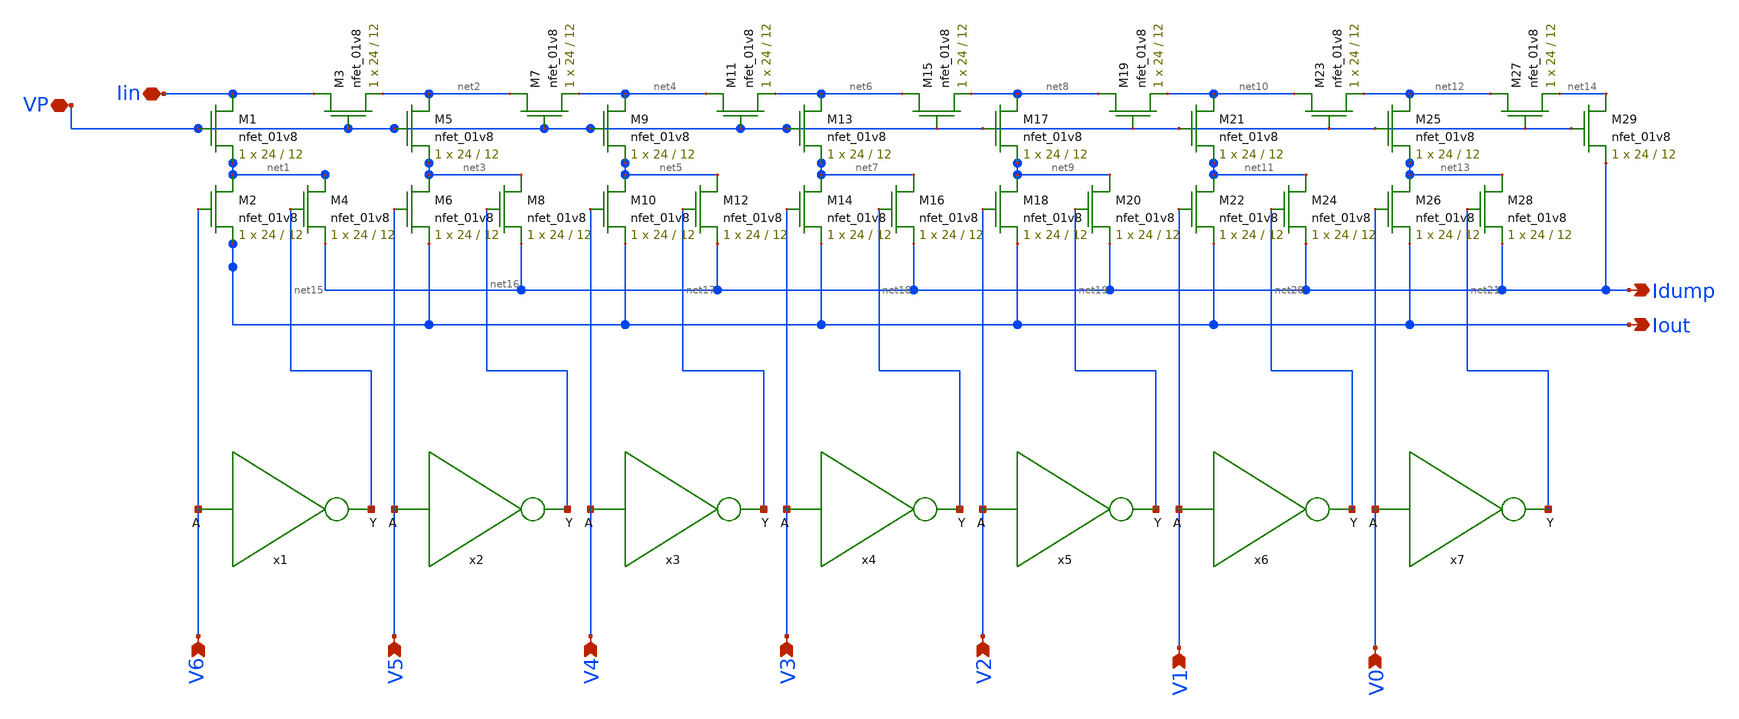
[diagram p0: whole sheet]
** sch_path: xschem/ladder.sch
**.subckt ladder V6 V5 V4 V3 V2 V1 V0 VP Iin Idump Iout
*.ipin V6
*.ipin V5
*.ipin V4
*.ipin V3
*.ipin V2
*.ipin V1
*.ipin V0
*.iopin VP
*.iopin Iin
*.opin Idump
*.opin Iout
XM1 Iin VP net1 GND sky130_fd_pr__nfet_01v8 L=12 W=24 nf=1 ad='int((nf+1)/2) * W/nf * 0.29' as='int((nf+2)/2) * W/nf * 0.29'
+ pd='2*int((nf+1)/2) * (W/nf + 0.29)' ps='2*int((nf+2)/2) * (W/nf + 0.29)' nrd='0.29 / W' nrs='0.29 / W'
+ sa=0 sb=0 sd=0 mult=1 m=1
XM3 Iin VP net2 GND sky130_fd_pr__nfet_01v8 L=12 W=24 nf=1 ad='int((nf+1)/2) * W/nf * 0.29' as='int((nf+2)/2) * W/nf * 0.29'
+ pd='2*int((nf+1)/2) * (W/nf + 0.29)' ps='2*int((nf+2)/2) * (W/nf + 0.29)' nrd='0.29 / W' nrs='0.29 / W'
+ sa=0 sb=0 sd=0 mult=1 m=1
XM5 net2 VP net3 GND sky130_fd_pr__nfet_01v8 L=12 W=24 nf=1 ad='int((nf+1)/2) * W/nf * 0.29' as='int((nf+2)/2) * W/nf * 0.29'
+ pd='2*int((nf+1)/2) * (W/nf + 0.29)' ps='2*int((nf+2)/2) * (W/nf + 0.29)' nrd='0.29 / W' nrs='0.29 / W'
+ sa=0 sb=0 sd=0 mult=1 m=1
XM7 net2 VP net4 GND sky130_fd_pr__nfet_01v8 L=12 W=24 nf=1 ad='int((nf+1)/2) * W/nf * 0.29' as='int((nf+2)/2) * W/nf * 0.29'
+ pd='2*int((nf+1)/2) * (W/nf + 0.29)' ps='2*int((nf+2)/2) * (W/nf + 0.29)' nrd='0.29 / W' nrs='0.29 / W'
+ sa=0 sb=0 sd=0 mult=1 m=1
XM6 net3 V5 Iout GND sky130_fd_pr__nfet_01v8 L=12 W=24 nf=1 ad='int((nf+1)/2) * W/nf * 0.29' as='int((nf+2)/2) * W/nf * 0.29'
+ pd='2*int((nf+1)/2) * (W/nf + 0.29)' ps='2*int((nf+2)/2) * (W/nf + 0.29)' nrd='0.29 / W' nrs='0.29 / W'
+ sa=0 sb=0 sd=0 mult=1 m=1
XM8 net3 net16 Idump GND sky130_fd_pr__nfet_01v8 L=12 W=24 nf=1 ad='int((nf+1)/2) * W/nf * 0.29' as='int((nf+2)/2) * W/nf * 0.29'
+ pd='2*int((nf+1)/2) * (W/nf + 0.29)' ps='2*int((nf+2)/2) * (W/nf + 0.29)' nrd='0.29 / W' nrs='0.29 / W'
+ sa=0 sb=0 sd=0 mult=1 m=1
XM2 net1 V6 Iout GND sky130_fd_pr__nfet_01v8 L=12 W=24 nf=1 ad='int((nf+1)/2) * W/nf * 0.29' as='int((nf+2)/2) * W/nf * 0.29'
+ pd='2*int((nf+1)/2) * (W/nf + 0.29)' ps='2*int((nf+2)/2) * (W/nf + 0.29)' nrd='0.29 / W' nrs='0.29 / W'
+ sa=0 sb=0 sd=0 mult=1 m=1
XM4 net1 net15 Idump GND sky130_fd_pr__nfet_01v8 L=12 W=24 nf=1 ad='int((nf+1)/2) * W/nf * 0.29' as='int((nf+2)/2) * W/nf * 0.29'
+ pd='2*int((nf+1)/2) * (W/nf + 0.29)' ps='2*int((nf+2)/2) * (W/nf + 0.29)' nrd='0.29 / W' nrs='0.29 / W'
+ sa=0 sb=0 sd=0 mult=1 m=1
XM9 net4 VP net5 GND sky130_fd_pr__nfet_01v8 L=12 W=24 nf=1 ad='int((nf+1)/2) * W/nf * 0.29' as='int((nf+2)/2) * W/nf * 0.29'
+ pd='2*int((nf+1)/2) * (W/nf + 0.29)' ps='2*int((nf+2)/2) * (W/nf + 0.29)' nrd='0.29 / W' nrs='0.29 / W'
+ sa=0 sb=0 sd=0 mult=1 m=1
XM11 net4 VP net6 GND sky130_fd_pr__nfet_01v8 L=12 W=24 nf=1 ad='int((nf+1)/2) * W/nf * 0.29' as='int((nf+2)/2) * W/nf * 0.29'
+ pd='2*int((nf+1)/2) * (W/nf + 0.29)' ps='2*int((nf+2)/2) * (W/nf + 0.29)' nrd='0.29 / W' nrs='0.29 / W'
+ sa=0 sb=0 sd=0 mult=1 m=1
XM10 net5 V4 Iout GND sky130_fd_pr__nfet_01v8 L=12 W=24 nf=1 ad='int((nf+1)/2) * W/nf * 0.29' as='int((nf+2)/2) * W/nf * 0.29'
+ pd='2*int((nf+1)/2) * (W/nf + 0.29)' ps='2*int((nf+2)/2) * (W/nf + 0.29)' nrd='0.29 / W' nrs='0.29 / W'
+ sa=0 sb=0 sd=0 mult=1 m=1
XM12 net5 net17 Idump GND sky130_fd_pr__nfet_01v8 L=12 W=24 nf=1 ad='int((nf+1)/2) * W/nf * 0.29' as='int((nf+2)/2) * W/nf * 0.29'
+ pd='2*int((nf+1)/2) * (W/nf + 0.29)' ps='2*int((nf+2)/2) * (W/nf + 0.29)' nrd='0.29 / W' nrs='0.29 / W'
+ sa=0 sb=0 sd=0 mult=1 m=1
XM13 net6 VP net7 GND sky130_fd_pr__nfet_01v8 L=12 W=24 nf=1 ad='int((nf+1)/2) * W/nf * 0.29' as='int((nf+2)/2) * W/nf * 0.29'
+ pd='2*int((nf+1)/2) * (W/nf + 0.29)' ps='2*int((nf+2)/2) * (W/nf + 0.29)' nrd='0.29 / W' nrs='0.29 / W'
+ sa=0 sb=0 sd=0 mult=1 m=1
XM15 net6 VP net8 GND sky130_fd_pr__nfet_01v8 L=12 W=24 nf=1 ad='int((nf+1)/2) * W/nf * 0.29' as='int((nf+2)/2) * W/nf * 0.29'
+ pd='2*int((nf+1)/2) * (W/nf + 0.29)' ps='2*int((nf+2)/2) * (W/nf + 0.29)' nrd='0.29 / W' nrs='0.29 / W'
+ sa=0 sb=0 sd=0 mult=1 m=1
XM14 net7 V3 Iout GND sky130_fd_pr__nfet_01v8 L=12 W=24 nf=1 ad='int((nf+1)/2) * W/nf * 0.29' as='int((nf+2)/2) * W/nf * 0.29'
+ pd='2*int((nf+1)/2) * (W/nf + 0.29)' ps='2*int((nf+2)/2) * (W/nf + 0.29)' nrd='0.29 / W' nrs='0.29 / W'
+ sa=0 sb=0 sd=0 mult=1 m=1
XM16 net7 net18 Idump GND sky130_fd_pr__nfet_01v8 L=12 W=24 nf=1 ad='int((nf+1)/2) * W/nf * 0.29' as='int((nf+2)/2) * W/nf * 0.29'
+ pd='2*int((nf+1)/2) * (W/nf + 0.29)' ps='2*int((nf+2)/2) * (W/nf + 0.29)' nrd='0.29 / W' nrs='0.29 / W'
+ sa=0 sb=0 sd=0 mult=1 m=1
XM17 net8 VP net9 GND sky130_fd_pr__nfet_01v8 L=12 W=24 nf=1 ad='int((nf+1)/2) * W/nf * 0.29' as='int((nf+2)/2) * W/nf * 0.29'
+ pd='2*int((nf+1)/2) * (W/nf + 0.29)' ps='2*int((nf+2)/2) * (W/nf + 0.29)' nrd='0.29 / W' nrs='0.29 / W'
+ sa=0 sb=0 sd=0 mult=1 m=1
XM19 net8 VP net10 GND sky130_fd_pr__nfet_01v8 L=12 W=24 nf=1 ad='int((nf+1)/2) * W/nf * 0.29' as='int((nf+2)/2) * W/nf * 0.29'
+ pd='2*int((nf+1)/2) * (W/nf + 0.29)' ps='2*int((nf+2)/2) * (W/nf + 0.29)' nrd='0.29 / W' nrs='0.29 / W'
+ sa=0 sb=0 sd=0 mult=1 m=1
XM18 net9 V2 Iout GND sky130_fd_pr__nfet_01v8 L=12 W=24 nf=1 ad='int((nf+1)/2) * W/nf * 0.29' as='int((nf+2)/2) * W/nf * 0.29'
+ pd='2*int((nf+1)/2) * (W/nf + 0.29)' ps='2*int((nf+2)/2) * (W/nf + 0.29)' nrd='0.29 / W' nrs='0.29 / W'
+ sa=0 sb=0 sd=0 mult=1 m=1
XM20 net9 net19 Idump GND sky130_fd_pr__nfet_01v8 L=12 W=24 nf=1 ad='int((nf+1)/2) * W/nf * 0.29' as='int((nf+2)/2) * W/nf * 0.29'
+ pd='2*int((nf+1)/2) * (W/nf + 0.29)' ps='2*int((nf+2)/2) * (W/nf + 0.29)' nrd='0.29 / W' nrs='0.29 / W'
+ sa=0 sb=0 sd=0 mult=1 m=1
XM21 net10 VP net11 GND sky130_fd_pr__nfet_01v8 L=12 W=24 nf=1 ad='int((nf+1)/2) * W/nf * 0.29' as='int((nf+2)/2) * W/nf * 0.29'
+ pd='2*int((nf+1)/2) * (W/nf + 0.29)' ps='2*int((nf+2)/2) * (W/nf + 0.29)' nrd='0.29 / W' nrs='0.29 / W'
+ sa=0 sb=0 sd=0 mult=1 m=1
XM23 net10 VP net12 GND sky130_fd_pr__nfet_01v8 L=12 W=24 nf=1 ad='int((nf+1)/2) * W/nf * 0.29' as='int((nf+2)/2) * W/nf * 0.29'
+ pd='2*int((nf+1)/2) * (W/nf + 0.29)' ps='2*int((nf+2)/2) * (W/nf + 0.29)' nrd='0.29 / W' nrs='0.29 / W'
+ sa=0 sb=0 sd=0 mult=1 m=1
XM22 net11 V1 Iout GND sky130_fd_pr__nfet_01v8 L=12 W=24 nf=1 ad='int((nf+1)/2) * W/nf * 0.29' as='int((nf+2)/2) * W/nf * 0.29'
+ pd='2*int((nf+1)/2) * (W/nf + 0.29)' ps='2*int((nf+2)/2) * (W/nf + 0.29)' nrd='0.29 / W' nrs='0.29 / W'
+ sa=0 sb=0 sd=0 mult=1 m=1
XM24 net11 net20 Idump GND sky130_fd_pr__nfet_01v8 L=12 W=24 nf=1 ad='int((nf+1)/2) * W/nf * 0.29' as='int((nf+2)/2) * W/nf * 0.29'
+ pd='2*int((nf+1)/2) * (W/nf + 0.29)' ps='2*int((nf+2)/2) * (W/nf + 0.29)' nrd='0.29 / W' nrs='0.29 / W'
+ sa=0 sb=0 sd=0 mult=1 m=1
XM25 net12 VP net13 GND sky130_fd_pr__nfet_01v8 L=12 W=24 nf=1 ad='int((nf+1)/2) * W/nf * 0.29' as='int((nf+2)/2) * W/nf * 0.29'
+ pd='2*int((nf+1)/2) * (W/nf + 0.29)' ps='2*int((nf+2)/2) * (W/nf + 0.29)' nrd='0.29 / W' nrs='0.29 / W'
+ sa=0 sb=0 sd=0 mult=1 m=1
XM27 net12 VP net14 GND sky130_fd_pr__nfet_01v8 L=12 W=24 nf=1 ad='int((nf+1)/2) * W/nf * 0.29' as='int((nf+2)/2) * W/nf * 0.29'
+ pd='2*int((nf+1)/2) * (W/nf + 0.29)' ps='2*int((nf+2)/2) * (W/nf + 0.29)' nrd='0.29 / W' nrs='0.29 / W'
+ sa=0 sb=0 sd=0 mult=1 m=1
XM26 net13 V0 Iout GND sky130_fd_pr__nfet_01v8 L=12 W=24 nf=1 ad='int((nf+1)/2) * W/nf * 0.29' as='int((nf+2)/2) * W/nf * 0.29'
+ pd='2*int((nf+1)/2) * (W/nf + 0.29)' ps='2*int((nf+2)/2) * (W/nf + 0.29)' nrd='0.29 / W' nrs='0.29 / W'
+ sa=0 sb=0 sd=0 mult=1 m=1
XM28 net13 net21 Idump GND sky130_fd_pr__nfet_01v8 L=12 W=24 nf=1 ad='int((nf+1)/2) * W/nf * 0.29' as='int((nf+2)/2) * W/nf * 0.29'
+ pd='2*int((nf+1)/2) * (W/nf + 0.29)' ps='2*int((nf+2)/2) * (W/nf + 0.29)' nrd='0.29 / W' nrs='0.29 / W'
+ sa=0 sb=0 sd=0 mult=1 m=1
XM29 net14 VP Idump GND sky130_fd_pr__nfet_01v8 L=12 W=24 nf=1 ad='int((nf+1)/2) * W/nf * 0.29' as='int((nf+2)/2) * W/nf * 0.29'
+ pd='2*int((nf+1)/2) * (W/nf + 0.29)' ps='2*int((nf+2)/2) * (W/nf + 0.29)' nrd='0.29 / W' nrs='0.29 / W'
+ sa=0 sb=0 sd=0 mult=1 m=1
x1 net15 V6 inverter
x2 net16 V5 inverter
x3 net17 V4 inverter
x4 net18 V3 inverter
x5 net19 V2 inverter
x6 net20 V1 inverter
x7 net21 V0 inverter
**.ends

* expanding   symbol:  ./inverter.sym # of pins=2
** sym_path: xschem/inverter.sym
** sch_path: xschem/inverter.sch
.subckt inverter Y A
*.ipin A
*.opin Y
XM1 Y A VDD VDD sky130_fd_pr__pfet_01v8 L=0.15 W=1 nf=1 ad='int((nf+1)/2) * W/nf * 0.29' as='int((nf+2)/2) * W/nf * 0.29'
+ pd='2*int((nf+1)/2) * (W/nf + 0.29)' ps='2*int((nf+2)/2) * (W/nf + 0.29)' nrd='0.29 / W' nrs='0.29 / W'
+ sa=0 sb=0 sd=0 mult=1 m=1
XM2 Y A GND GND sky130_fd_pr__nfet_01v8 L=0.15 W=1 nf=1 ad='int((nf+1)/2) * W/nf * 0.29' as='int((nf+2)/2) * W/nf * 0.29'
+ pd='2*int((nf+1)/2) * (W/nf + 0.29)' ps='2*int((nf+2)/2) * (W/nf + 0.29)' nrd='0.29 / W' nrs='0.29 / W'
+ sa=0 sb=0 sd=0 mult=1 m=1
.ends

.GLOBAL GND
.GLOBAL VDD
.end
